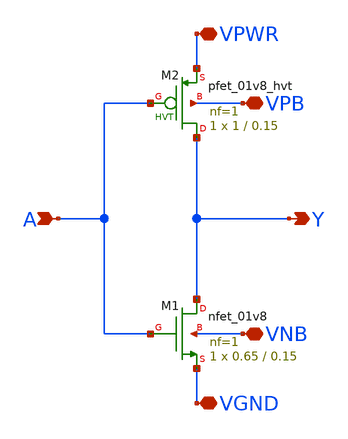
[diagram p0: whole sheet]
** sch_path: tests/golden/SCHEM/cases/SCHEM-LVS-01/input/inv_1.sch
**.subckt inv_1 A Y VPWR VPB VGND VNB
*.ipin A
*.opin Y
*.iopin VPWR
*.iopin VPB
*.iopin VGND
*.iopin VNB
XM2 Y A VPWR VPB sky130_fd_pr__pfet_01v8_hvt L=0.15 W=1 nf=1 ad='int((1 + 1)/2) * 1 / 1 * 0.29' as='int((1 + 2)/2) * 1 / 1 * 0.29'
+ pd='2*int((1 + 1)/2) * (1 / 1 + 0.29)' ps='2*int((1 + 2)/2) * (1 / 1 + 0.29)' nrd='0.29 / 1 ' nrs='0.29 / 1 '
+ sa=0 sb=0 sd=0 mult=1 m=1
XM1 Y A VGND VNB sky130_fd_pr__nfet_01v8 L=0.15 W=0.65 nf=1 ad='int((1 + 1)/2) * 0.65 / 1 * 0.29' as='int((1 + 2)/2) * 0.65 / 1 * 0.29'
+ pd='2*int((1 + 1)/2) * (0.65 / 1 + 0.29)' ps='2*int((1 + 2)/2) * (0.65 / 1 + 0.29)' nrd='0.29 / 0.65 '
+ nrs='0.29 / 0.65 ' sa=0 sb=0 sd=0 mult=1 m=1
**.ends
.end
